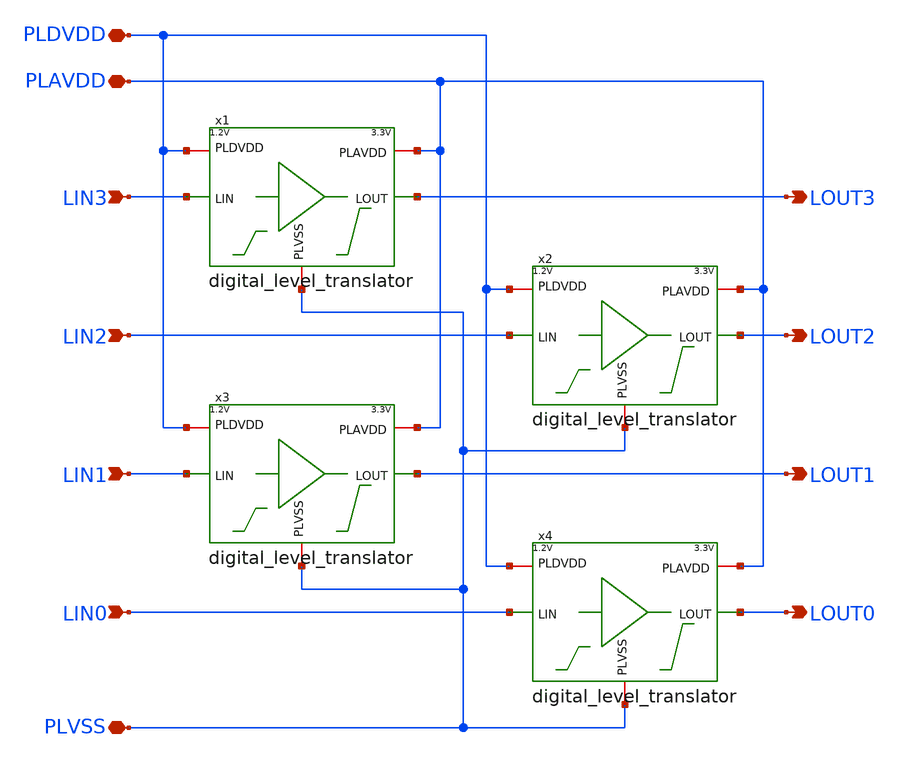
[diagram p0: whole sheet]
** sch_path: xschem/4x_digital_level_translator.sch
**.subckt 4x_digital_level_translator PLDVDD PLAVDD PLVSS LIN3 LIN2 LIN1 LIN0 LOUT3 LOUT2 LOUT1
*+ LOUT0
*.iopin PLDVDD
*.iopin PLAVDD
*.iopin PLVSS
*.ipin LIN3
*.ipin LIN2
*.ipin LIN1
*.ipin LIN0
*.opin LOUT3
*.opin LOUT2
*.opin LOUT1
*.opin LOUT0
x1 PLAVDD PLDVDD LIN3 LOUT3 PLVSS digital_level_translator
x2 PLAVDD PLDVDD LIN2 LOUT2 PLVSS digital_level_translator
x3 PLAVDD PLDVDD LIN1 LOUT1 PLVSS digital_level_translator
x4 PLAVDD PLDVDD LIN0 LOUT0 PLVSS digital_level_translator
**.ends

* expanding   symbol:  digital_level_translator.sym # of pins=5
** sym_path: xschem/digital_level_translator.sym
** sch_path: xschem/digital_level_translator.sch
.subckt digital_level_translator PLAVDD PLDVDD LIN LOUT PLVSS
*.iopin PLAVDD
*.iopin PLVSS
*.iopin PLDVDD
*.ipin LIN
*.opin LOUT
XM1 n_lin_buf LIN PLVSS PLVSS sg13_lv_nmos w=0.15u l=0.13u ng=1 m=1 mm_ok=1
XM2 n_lin_buf LIN PLDVDD PLDVDD sg13_lv_pmos w=0.3u l=0.13u ng=1 m=1 mm_ok=1
XM3 lin_buf n_lin_buf PLVSS PLVSS sg13_lv_nmos w=0.15u l=0.13u ng=1 m=1 mm_ok=1
XM4 lin_buf n_lin_buf PLDVDD PLDVDD sg13_lv_pmos w=0.3u l=0.13u ng=1 m=1 mm_ok=1
XM5 q_unbf n_lin_buf PLVSS PLVSS sg13_hv_nmos w=1u l=0.45u ng=1 m=1 mm_ok=1
XM6 n_q_unbf lin_buf PLVSS PLVSS sg13_hv_nmos w=1u l=0.45u ng=1 m=1 mm_ok=1
XM7 n_q_unbf q_unbf PLAVDD PLAVDD sg13_hv_pmos w=0.3u l=0.45u ng=1 m=1 mm_ok=1
XM9 LOUT n_q_unbf PLVSS PLVSS sg13_hv_nmos w=0.3u l=0.45u ng=1 m=4 mm_ok=1
XM10 LOUT n_q_unbf PLAVDD PLAVDD sg13_hv_pmos w=0.6u l=0.45u ng=1 m=4 mm_ok=1
XM8 q_unbf n_q_unbf PLAVDD PLAVDD sg13_hv_pmos w=0.3u l=0.45u ng=1 m=1 mm_ok=1
.ends

.end
